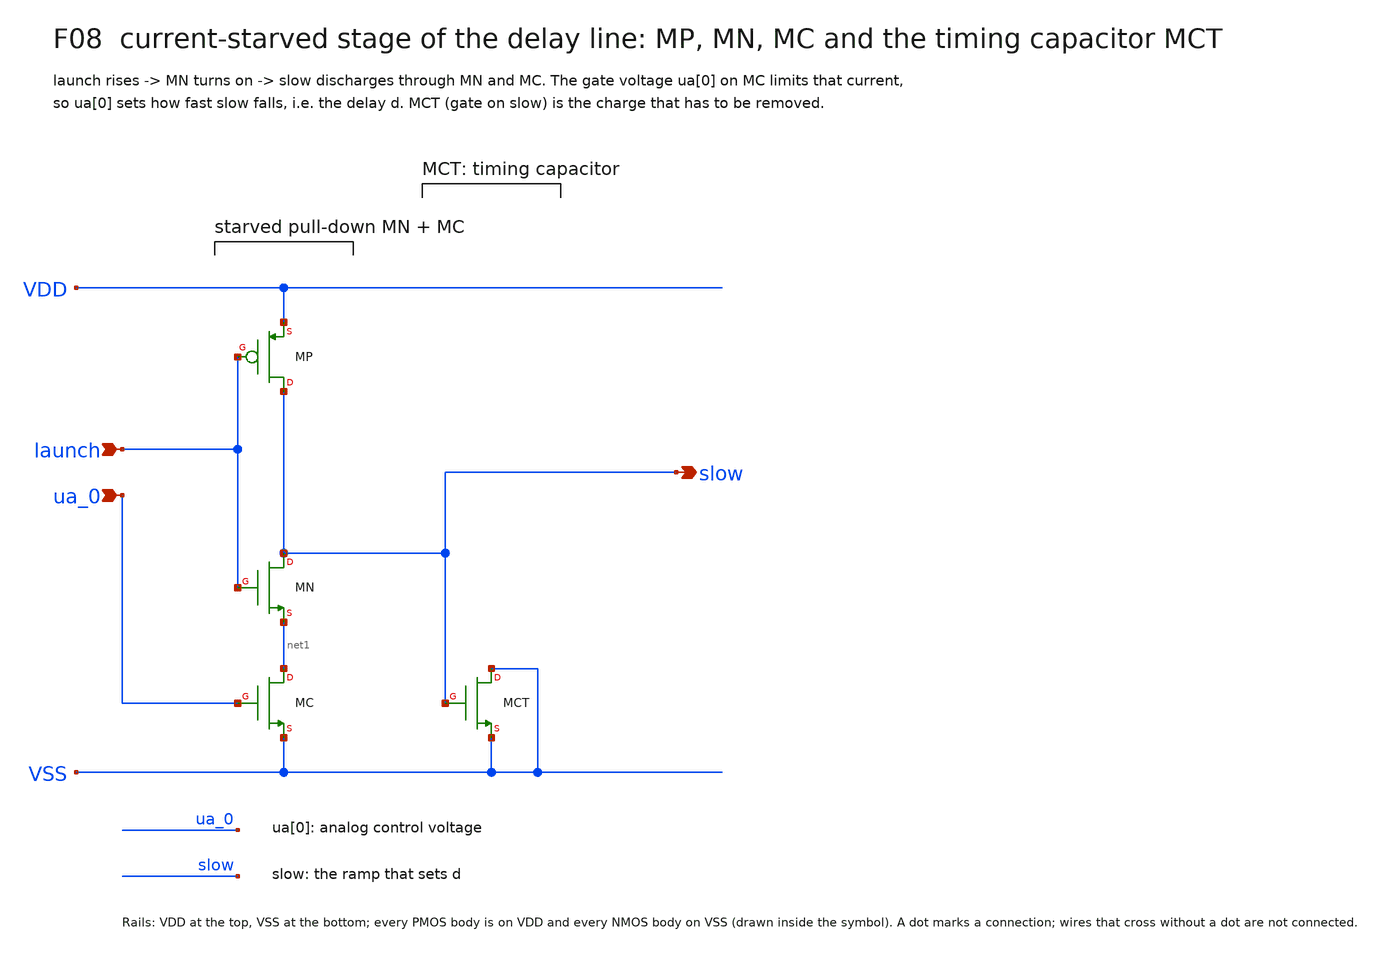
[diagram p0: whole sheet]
** sch_path: xschem/focus/F08_current_starved_stage.sch
**.subckt F08_current_starved_stage launch ua_0 slow
*.ipin launch
*.ipin ua_0
*.opin slow
XMP slow launch VDD VDD pfet_05v0 L=0.5u W=1.22u nf=1 m=1
XMN slow launch net1 VSS nfet_05v0 L=0.6u W=0.82u nf=1 m=1
XMC net1 ua_0 VSS VSS nfet_05v0 L=0.6u W=0.36u nf=1 m=1
XMCT VSS slow VSS VSS nfet_05v0 L=1u W=0.82u nf=1 m=1
**.ends
.end
